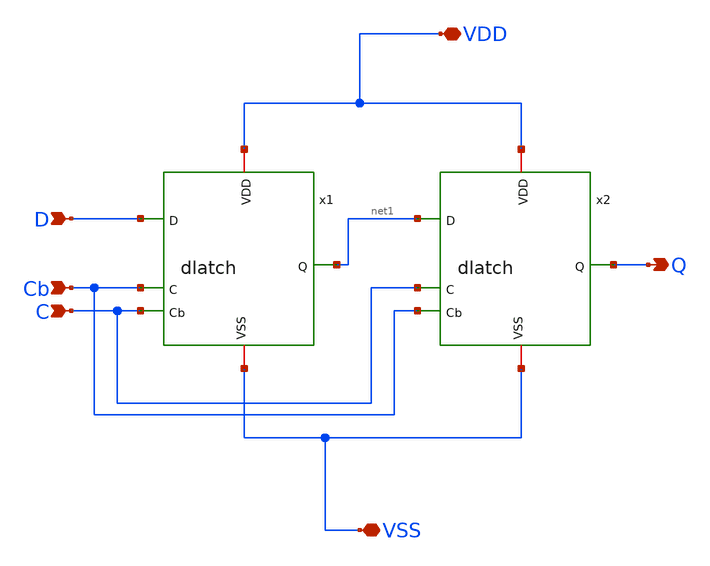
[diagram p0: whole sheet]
** sch_path: reg.sch
**.subckt reg C Cb D Q VDD VSS
*.ipin C
*.ipin Cb
*.ipin D
*.opin Q
*.iopin VDD
*.iopin VSS
x1 VDD Cb C D net1 VSS dlatch
x2 VDD C Cb net1 Q VSS dlatch
**.ends

* expanding   symbol:  xchem/xchem/dlatch.sym # of pins=6
** sym_path: dlatch.sym
** sch_path: dlatch.sch
.subckt dlatch VDD C Cb D Q VSS
*.ipin C
*.ipin Cb
*.ipin D
*.opin Q
*.iopin VDD
*.iopin VSS
x1 VDD net2 net1 C Cb VSS D mux
x2 VDD net1 Q VSS inverter
x3 VDD Q net2 VSS inverter
.ends


* expanding   symbol:  xchem/xchem/mux.sym # of pins=7
** sym_path: mux.sym
** sch_path: mux.sch
.subckt mux VDD D1 Y S Sb VSS D0
*.ipin S
*.ipin Sb
*.ipin D0
*.ipin D1
*.iopin VDD
*.iopin VSS
*.iopin Y
XM1 Y Sb D1 VDD sg13_lv_pmos w=0.15u l=0.13u ng=1 m=1 mm_ok=1
XM2 D0 S Y VDD sg13_lv_pmos w=0.15u l=0.13u ng=1 m=1 mm_ok=1
XM3 Y S D1 VSS sg13_lv_nmos w=0.15u l=0.13u ng=1 m=1 mm_ok=1
XM4 D0 Sb Y VSS sg13_lv_nmos w=0.15u l=0.13u ng=1 m=1 mm_ok=1
.ends


* expanding   symbol:  xchem/xchem/inverter.sym # of pins=4
** sym_path: inverter.sym
** sch_path: inverter.sch
.subckt inverter VDD A Y VSS
*.ipin A
*.iopin VDD
*.iopin VSS
*.opin Y
XM1 Y A VDD VDD sg13_lv_pmos w=0.15u l=0.13u ng=1 m=1 mm_ok=1
XM2 Y A VSS VSS sg13_lv_nmos w=0.15u l=0.13u ng=1 m=1 mm_ok=1
.ends

.end
